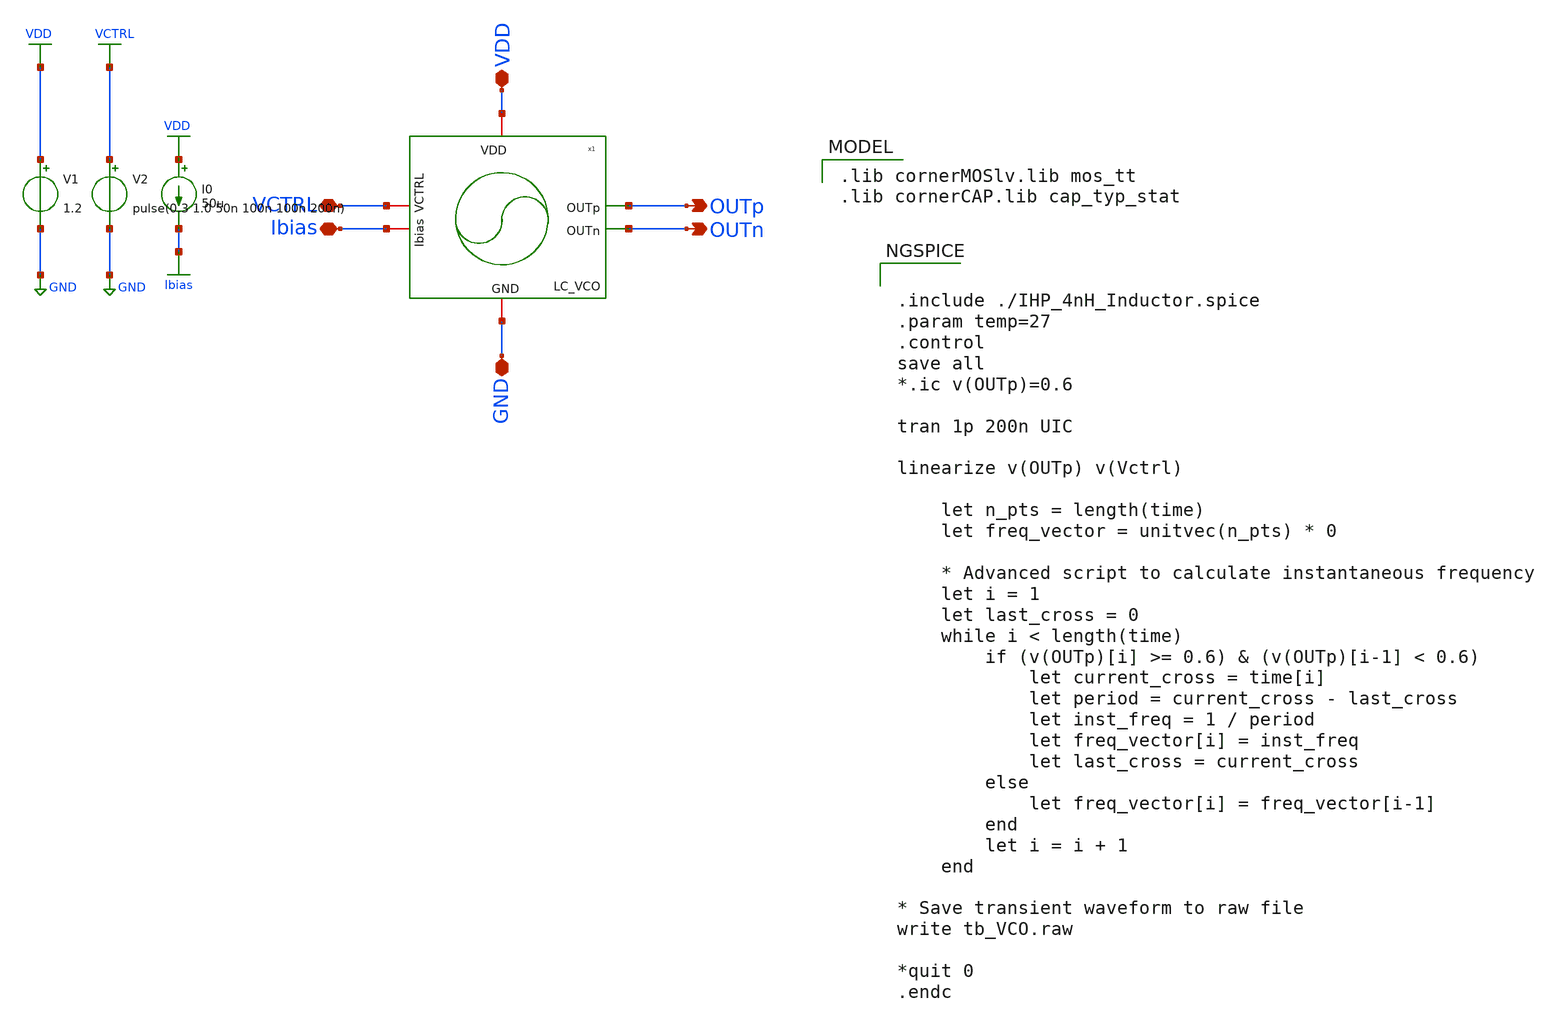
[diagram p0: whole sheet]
** sch_path: schematic/blocks/top-pll/LC_VCO_sweep_tb.sch
**.subckt LC_VCO_sweep_tb OUTp OUTn VDD VCTRL GND Ibias
*.opin OUTp
*.opin OUTn
*.iopin VDD
*.iopin VCTRL
*.iopin GND
*.iopin Ibias
V1 VDD GND 1.2
x1 VDD OUTp OUTn Ibias VCTRL GND LC_VCO
I0 VDD Ibias 50u
V2 VCTRL GND pulse(0.3 1.0 50n 100n 100n 200n)
**** begin user architecture code
 .lib cornerMOSlv.lib mos_tt
.lib cornerCAP.lib cap_typ_stat


.include ./IHP_4nH_Inductor.spice
.param temp=27
.control
save all
*.ic v(OUTp)=0.6

tran 1p 200n UIC

linearize v(OUTp) v(Vctrl)

    let n_pts = length(time)
    let freq_vector = unitvec(n_pts) * 0

    * Advanced script to calculate instantaneous frequency
    let i = 1
    let last_cross = 0
    while i < length(time)
        if (v(OUTp)[i] >= 0.6) & (v(OUTp)[i-1] < 0.6)
            let current_cross = time[i]
            let period = current_cross - last_cross
            let inst_freq = 1 / period
            let freq_vector[i] = inst_freq
            let last_cross = current_cross
        else
            let freq_vector[i] = freq_vector[i-1]
        end
        let i = i + 1
    end

* Save transient waveform to raw file
write tb_VCO.raw

*quit 0
.endc


**** end user architecture code
**.ends
.GLOBAL GND
.GLOBAL VDD
.GLOBAL VCTRL
.GLOBAL Ibias
.end
